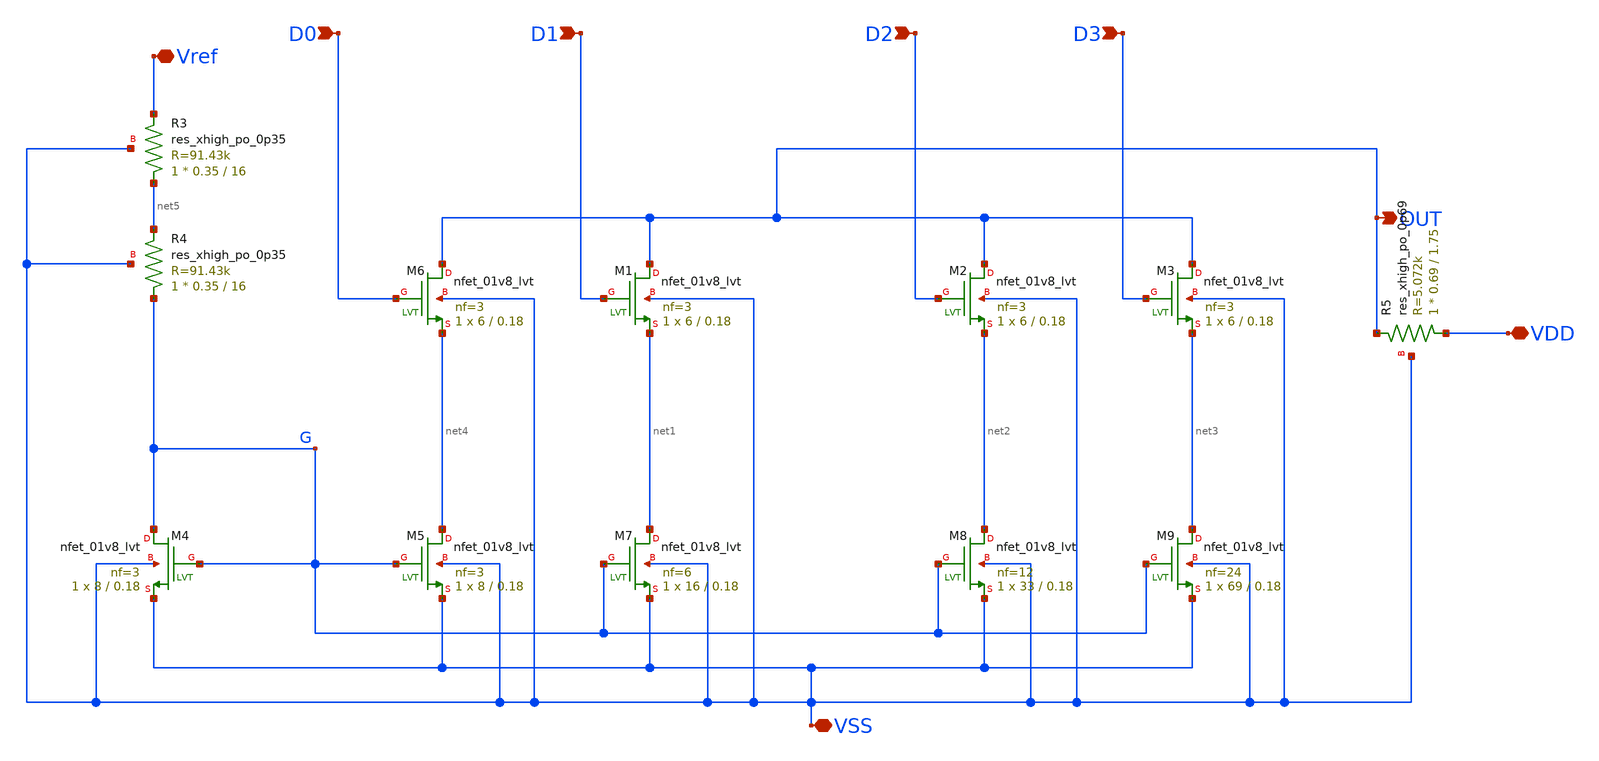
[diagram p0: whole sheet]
** sch_path: tt_um_DAC1/xschem/DAC.sch
**.subckt DAC D0 D1 D2 D3 Vref OUT VDD VSS
*.ipin D0
*.ipin D1
*.ipin D2
*.ipin D3
*.iopin Vref
*.opin OUT
*.iopin VDD
*.iopin VSS
XR3 net5 Vref VSS sky130_fd_pr__res_xhigh_po_0p35 L=16 mult=1 m=1
XR4 G net5 VSS sky130_fd_pr__res_xhigh_po_0p35 L=16 mult=1 m=1
XR5 VDD OUT VSS sky130_fd_pr__res_xhigh_po_0p69 L=1.75 mult=1 m=1
XM6 OUT D0 net4 VSS sky130_fd_pr__nfet_01v8_lvt L=0.18 W=6 nf=3 ad='int((3 + 1)/2) * 6 / 3 * 0.29' as='int((3 + 2)/2) * 6 / 3 * 0.29'
+ pd='2*int((3 + 1)/2) * (6 / 3 + 0.29)' ps='2*int((3 + 2)/2) * (6 / 3 + 0.29)' nrd='0.29 / 6 ' nrs='0.29 / 6 '
+ sa=0 sb=0 sd=0 mult=1 m=1
XM1 OUT D1 net1 VSS sky130_fd_pr__nfet_01v8_lvt L=0.18 W=6 nf=3 ad='int((3 + 1)/2) * 6 / 3 * 0.29' as='int((3 + 2)/2) * 6 / 3 * 0.29'
+ pd='2*int((3 + 1)/2) * (6 / 3 + 0.29)' ps='2*int((3 + 2)/2) * (6 / 3 + 0.29)' nrd='0.29 / 6 ' nrs='0.29 / 6 '
+ sa=0 sb=0 sd=0 mult=1 m=1
XM2 OUT D2 net2 VSS sky130_fd_pr__nfet_01v8_lvt L=0.18 W=6 nf=3 ad='int((3 + 1)/2) * 6 / 3 * 0.29' as='int((3 + 2)/2) * 6 / 3 * 0.29'
+ pd='2*int((3 + 1)/2) * (6 / 3 + 0.29)' ps='2*int((3 + 2)/2) * (6 / 3 + 0.29)' nrd='0.29 / 6 ' nrs='0.29 / 6 '
+ sa=0 sb=0 sd=0 mult=1 m=1
XM3 OUT D3 net3 VSS sky130_fd_pr__nfet_01v8_lvt L=0.18 W=6 nf=3 ad='int((3 + 1)/2) * 6 / 3 * 0.29' as='int((3 + 2)/2) * 6 / 3 * 0.29'
+ pd='2*int((3 + 1)/2) * (6 / 3 + 0.29)' ps='2*int((3 + 2)/2) * (6 / 3 + 0.29)' nrd='0.29 / 6 ' nrs='0.29 / 6 '
+ sa=0 sb=0 sd=0 mult=1 m=1
XM4 G G VSS VSS sky130_fd_pr__nfet_01v8_lvt L=0.18 W=8 nf=3 ad='int((3 + 1)/2) * 8 / 3 * 0.29' as='int((3 + 2)/2) * 8 / 3 * 0.29'
+ pd='2*int((3 + 1)/2) * (8 / 3 + 0.29)' ps='2*int((3 + 2)/2) * (8 / 3 + 0.29)' nrd='0.29 / 8 ' nrs='0.29 / 8 '
+ sa=0 sb=0 sd=0 mult=1 m=1
XM5 net4 G VSS VSS sky130_fd_pr__nfet_01v8_lvt L=0.18 W=8 nf=3 ad='int((3 + 1)/2) * 8 / 3 * 0.29' as='int((3 + 2)/2) * 8 / 3 * 0.29'
+ pd='2*int((3 + 1)/2) * (8 / 3 + 0.29)' ps='2*int((3 + 2)/2) * (8 / 3 + 0.29)' nrd='0.29 / 8 ' nrs='0.29 / 8 '
+ sa=0 sb=0 sd=0 mult=1 m=1
XM7 net1 G VSS VSS sky130_fd_pr__nfet_01v8_lvt L=0.18 W=16 nf=6 ad='int((6 + 1)/2) * 16 / 6 * 0.29' as='int((6 + 2)/2) * 16 / 6 * 0.29'
+ pd='2*int((6 + 1)/2) * (16 / 6 + 0.29)' ps='2*int((6 + 2)/2) * (16 / 6 + 0.29)' nrd='0.29 / 16 ' nrs='0.29 / 16 '
+ sa=0 sb=0 sd=0 mult=1 m=1
XM8 net2 G VSS VSS sky130_fd_pr__nfet_01v8_lvt L=0.18 W=33 nf=12 ad='int((12 + 1)/2) * 33 / 12 * 0.29'
+ as='int((12 + 2)/2) * 33 / 12 * 0.29' pd='2*int((12 + 1)/2) * (33 / 12 + 0.29)' ps='2*int((12 + 2)/2) * (33 / 12 + 0.29)'
+ nrd='0.29 / 33 ' nrs='0.29 / 33 ' sa=0 sb=0 sd=0 mult=1 m=1
XM9 net3 G VSS VSS sky130_fd_pr__nfet_01v8_lvt L=0.18 W=69 nf=24 ad='int((24 + 1)/2) * 69 / 24 * 0.29'
+ as='int((24 + 2)/2) * 69 / 24 * 0.29' pd='2*int((24 + 1)/2) * (69 / 24 + 0.29)' ps='2*int((24 + 2)/2) * (69 / 24 + 0.29)'
+ nrd='0.29 / 69 ' nrs='0.29 / 69 ' sa=0 sb=0 sd=0 mult=1 m=1
**.ends
.end
